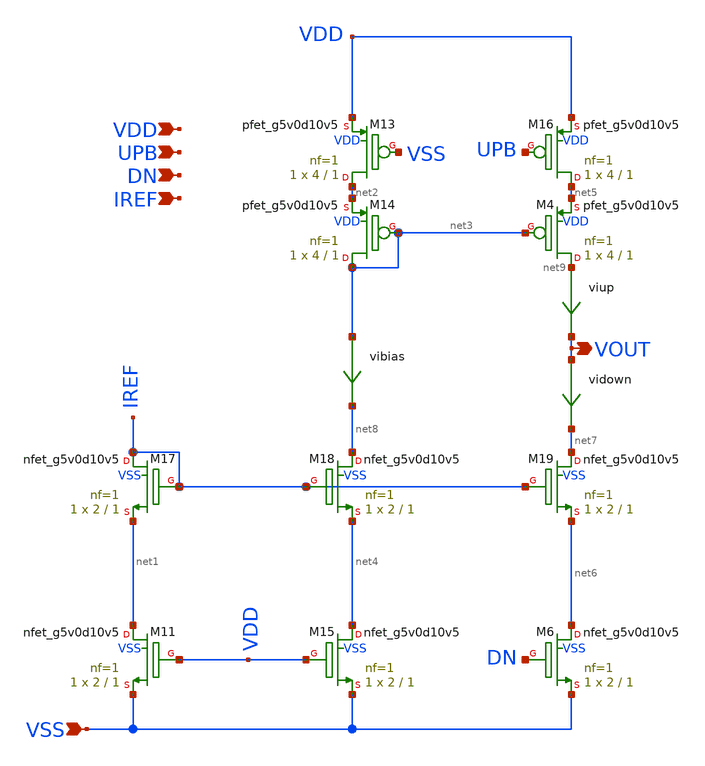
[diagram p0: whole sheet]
** sch_path: xschem/pll_cp_echo_hv.sch
**.subckt pll_cp_echo_hv VOUT VSS VDD DN UPB IREF
*.opin VOUT
*.ipin VSS
*.ipin VDD
*.ipin DN
*.ipin UPB
*.ipin IREF
vibias net3 net8 0
.save i(vibias)
XM16 net5 UPB VDD VDD sky130_fd_pr__pfet_g5v0d10v5 L=1 W=4 nf=1 ad='int((nf+1)/2) * W/nf * 0.29' as='int((nf+2)/2) * W/nf * 0.29'
+ pd='2*int((nf+1)/2) * (W/nf + 0.29)' ps='2*int((nf+2)/2) * (W/nf + 0.29)' nrd='0.29 / W' nrs='0.29 / W'
+ sa=0 sb=0 sd=0 mult=1 m=1
XM13 net2 VSS VDD VDD sky130_fd_pr__pfet_g5v0d10v5 L=1 W=4 nf=1 ad='int((nf+1)/2) * W/nf * 0.29' as='int((nf+2)/2) * W/nf * 0.29'
+ pd='2*int((nf+1)/2) * (W/nf + 0.29)' ps='2*int((nf+2)/2) * (W/nf + 0.29)' nrd='0.29 / W' nrs='0.29 / W'
+ sa=0 sb=0 sd=0 mult=1 m=1
XM14 net3 net3 net2 VDD sky130_fd_pr__pfet_g5v0d10v5 L=1 W=4 nf=1 ad='int((nf+1)/2) * W/nf * 0.29' as='int((nf+2)/2) * W/nf * 0.29'
+ pd='2*int((nf+1)/2) * (W/nf + 0.29)' ps='2*int((nf+2)/2) * (W/nf + 0.29)' nrd='0.29 / W' nrs='0.29 / W'
+ sa=0 sb=0 sd=0 mult=1 m=1
XM11 net1 VDD VSS VSS sky130_fd_pr__nfet_g5v0d10v5 L=1 W=2 nf=1 ad='int((nf+1)/2) * W/nf * 0.29' as='int((nf+2)/2) * W/nf * 0.29'
+ pd='2*int((nf+1)/2) * (W/nf + 0.29)' ps='2*int((nf+2)/2) * (W/nf + 0.29)' nrd='0.29 / W' nrs='0.29 / W'
+ sa=0 sb=0 sd=0 mult=1 m=1
XM17 IREF IREF net1 VSS sky130_fd_pr__nfet_g5v0d10v5 L=1 W=2 nf=1 ad='int((nf+1)/2) * W/nf * 0.29' as='int((nf+2)/2) * W/nf * 0.29'
+ pd='2*int((nf+1)/2) * (W/nf + 0.29)' ps='2*int((nf+2)/2) * (W/nf + 0.29)' nrd='0.29 / W' nrs='0.29 / W'
+ sa=0 sb=0 sd=0 mult=1 m=1
XM15 net4 VDD VSS VSS sky130_fd_pr__nfet_g5v0d10v5 L=1 W=2 nf=1 ad='int((nf+1)/2) * W/nf * 0.29' as='int((nf+2)/2) * W/nf * 0.29'
+ pd='2*int((nf+1)/2) * (W/nf + 0.29)' ps='2*int((nf+2)/2) * (W/nf + 0.29)' nrd='0.29 / W' nrs='0.29 / W'
+ sa=0 sb=0 sd=0 mult=1 m=1
XM18 net8 IREF net4 VSS sky130_fd_pr__nfet_g5v0d10v5 L=1 W=2 nf=1 ad='int((nf+1)/2) * W/nf * 0.29' as='int((nf+2)/2) * W/nf * 0.29'
+ pd='2*int((nf+1)/2) * (W/nf + 0.29)' ps='2*int((nf+2)/2) * (W/nf + 0.29)' nrd='0.29 / W' nrs='0.29 / W'
+ sa=0 sb=0 sd=0 mult=1 m=1
XM6 net6 DN VSS VSS sky130_fd_pr__nfet_g5v0d10v5 L=1 W=2 nf=1 ad='int((nf+1)/2) * W/nf * 0.29' as='int((nf+2)/2) * W/nf * 0.29'
+ pd='2*int((nf+1)/2) * (W/nf + 0.29)' ps='2*int((nf+2)/2) * (W/nf + 0.29)' nrd='0.29 / W' nrs='0.29 / W'
+ sa=0 sb=0 sd=0 mult=1 m=1
XM19 net7 IREF net6 VSS sky130_fd_pr__nfet_g5v0d10v5 L=1 W=2 nf=1 ad='int((nf+1)/2) * W/nf * 0.29' as='int((nf+2)/2) * W/nf * 0.29'
+ pd='2*int((nf+1)/2) * (W/nf + 0.29)' ps='2*int((nf+2)/2) * (W/nf + 0.29)' nrd='0.29 / W' nrs='0.29 / W'
+ sa=0 sb=0 sd=0 mult=1 m=1
XM4 net9 net3 net5 VDD sky130_fd_pr__pfet_g5v0d10v5 L=1 W=4 nf=1 ad='int((nf+1)/2) * W/nf * 0.29' as='int((nf+2)/2) * W/nf * 0.29'
+ pd='2*int((nf+1)/2) * (W/nf + 0.29)' ps='2*int((nf+2)/2) * (W/nf + 0.29)' nrd='0.29 / W' nrs='0.29 / W'
+ sa=0 sb=0 sd=0 mult=1 m=1
viup net9 VOUT 0
.save i(viup)
vidown VOUT net7 0
.save i(vidown)
**.ends
.end
